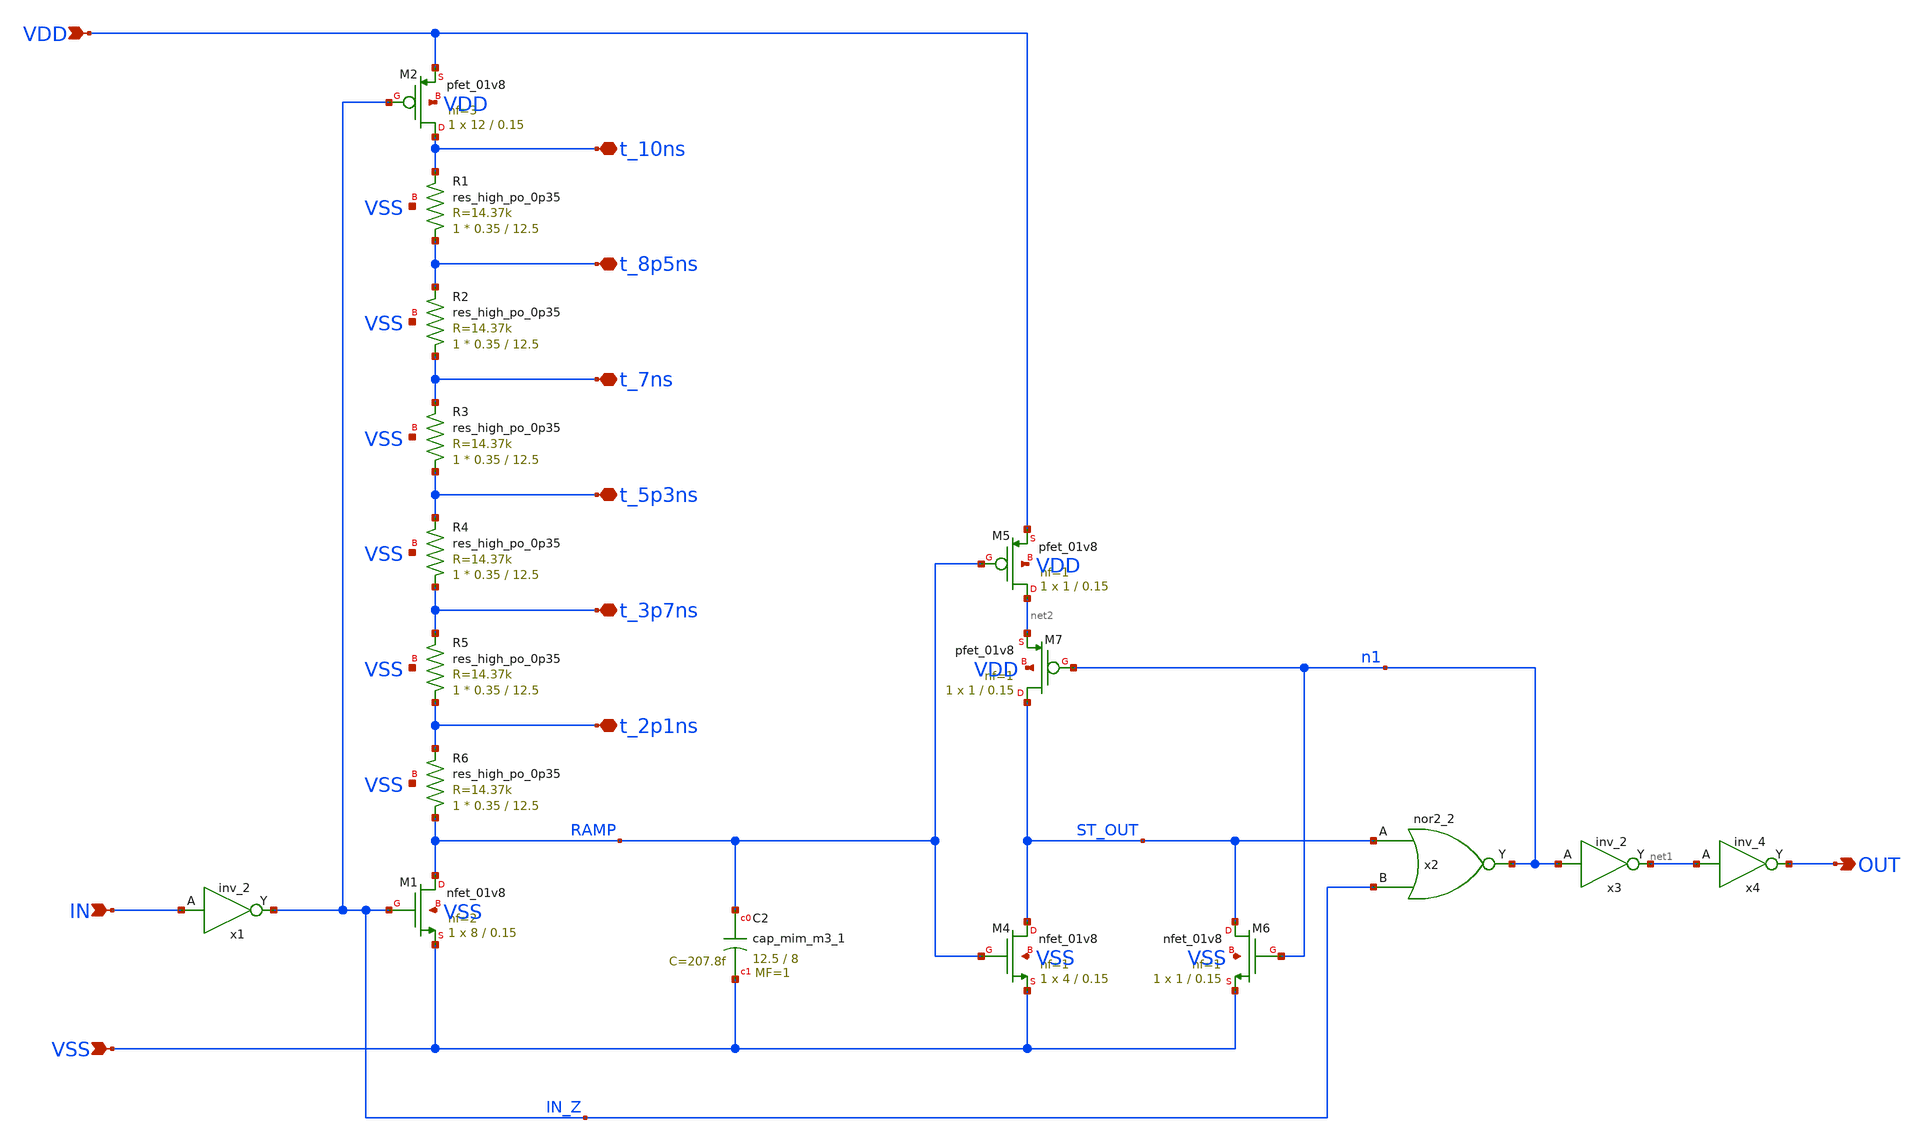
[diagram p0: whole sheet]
** sch_path: delay_cell/delay_cell.sch
**.subckt delay_cell OUT t_10ns t_8p5ns t_7ns t_5p3ns t_3p7ns t_2p1ns VSS IN VDD
*.opin OUT
*.iopin t_10ns
*.iopin t_8p5ns
*.iopin t_7ns
*.iopin t_5p3ns
*.iopin t_3p7ns
*.iopin t_2p1ns
*.ipin VSS
*.ipin IN
*.ipin VDD
XM1 RAMP IN_Z VSS VSS sky130_fd_pr__nfet_01v8 L=0.15 W=8 nf=2 ad='int((nf+1)/2) * W/nf * 0.29' as='int((nf+2)/2) * W/nf * 0.29'
+ pd='2*int((nf+1)/2) * (W/nf + 0.29)' ps='2*int((nf+2)/2) * (W/nf + 0.29)' nrd='0.29 / W' nrs='0.29 / W'
+ sa=0 sb=0 sd=0 mult=1 m=1
XM2 t_10ns IN_Z VDD VDD sky130_fd_pr__pfet_01v8 L=0.15 W=12 nf=3 ad='int((nf+1)/2) * W/nf * 0.29' as='int((nf+2)/2) * W/nf * 0.29'
+ pd='2*int((nf+1)/2) * (W/nf + 0.29)' ps='2*int((nf+2)/2) * (W/nf + 0.29)' nrd='0.29 / W' nrs='0.29 / W'
+ sa=0 sb=0 sd=0 mult=1 m=1
XR1 t_8p5ns t_10ns VSS sky130_fd_pr__res_high_po_0p35 L=12.5 mult=1 m=1
XR2 t_7ns t_8p5ns VSS sky130_fd_pr__res_high_po_0p35 L=12.5 mult=1 m=1
XR3 t_5p3ns t_7ns VSS sky130_fd_pr__res_high_po_0p35 L=12.5 mult=1 m=1
XR4 t_3p7ns t_5p3ns VSS sky130_fd_pr__res_high_po_0p35 L=12.5 mult=1 m=1
XR5 t_2p1ns t_3p7ns VSS sky130_fd_pr__res_high_po_0p35 L=12.5 mult=1 m=1
x1 IN VSS VSS VDD VDD IN_Z sky130_fd_sc_hd__inv_2
XM4 ST_OUT RAMP VSS VSS sky130_fd_pr__nfet_01v8 L=0.15 W=4 nf=1 ad='int((nf+1)/2) * W/nf * 0.29' as='int((nf+2)/2) * W/nf * 0.29'
+ pd='2*int((nf+1)/2) * (W/nf + 0.29)' ps='2*int((nf+2)/2) * (W/nf + 0.29)' nrd='0.29 / W' nrs='0.29 / W'
+ sa=0 sb=0 sd=0 mult=1 m=1
XM5 net2 RAMP VDD VDD sky130_fd_pr__pfet_01v8 L=0.15 W=1 nf=1 ad='int((nf+1)/2) * W/nf * 0.29' as='int((nf+2)/2) * W/nf * 0.29'
+ pd='2*int((nf+1)/2) * (W/nf + 0.29)' ps='2*int((nf+2)/2) * (W/nf + 0.29)' nrd='0.29 / W' nrs='0.29 / W'
+ sa=0 sb=0 sd=0 mult=1 m=1
XM6 ST_OUT n1 VSS VSS sky130_fd_pr__nfet_01v8 L=0.15 W=1 nf=1 ad='int((nf+1)/2) * W/nf * 0.29' as='int((nf+2)/2) * W/nf * 0.29'
+ pd='2*int((nf+1)/2) * (W/nf + 0.29)' ps='2*int((nf+2)/2) * (W/nf + 0.29)' nrd='0.29 / W' nrs='0.29 / W'
+ sa=0 sb=0 sd=0 mult=1 m=1
x2 ST_OUT IN_Z VSS VSS VDD VDD n1 sky130_fd_sc_hd__nor2_2
x3 n1 VSS VSS VDD VDD net1 sky130_fd_sc_hd__inv_2
x4 net1 VSS VSS VDD VDD OUT sky130_fd_sc_hd__inv_4
XR6 RAMP t_2p1ns VSS sky130_fd_pr__res_high_po_0p35 L=12.5 mult=1 m=1
XM7 ST_OUT n1 net2 VDD sky130_fd_pr__pfet_01v8 L=0.15 W=1 nf=1 ad='int((nf+1)/2) * W/nf * 0.29' as='int((nf+2)/2) * W/nf * 0.29'
+ pd='2*int((nf+1)/2) * (W/nf + 0.29)' ps='2*int((nf+2)/2) * (W/nf + 0.29)' nrd='0.29 / W' nrs='0.29 / W'
+ sa=0 sb=0 sd=0 mult=1 m=1
XC2 RAMP VSS sky130_fd_pr__cap_mim_m3_1 W=12.5 L=8 MF=1 m=1
**.ends
.end
